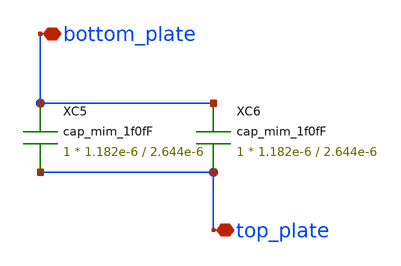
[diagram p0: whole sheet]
** sch_path: CDAC/2C.sch
**.subckt 2C top_plate bottom_plate
*.iopin top_plate
*.iopin bottom_plate
XC5 bottom_plate top_plate cap_mim_1f0fF c_width=1.182e-6 c_length=2.644e-6 m=1
XC6 bottom_plate top_plate cap_mim_1f0fF c_width=1.182e-6 c_length=2.644e-6 m=1
**.ends
.end
